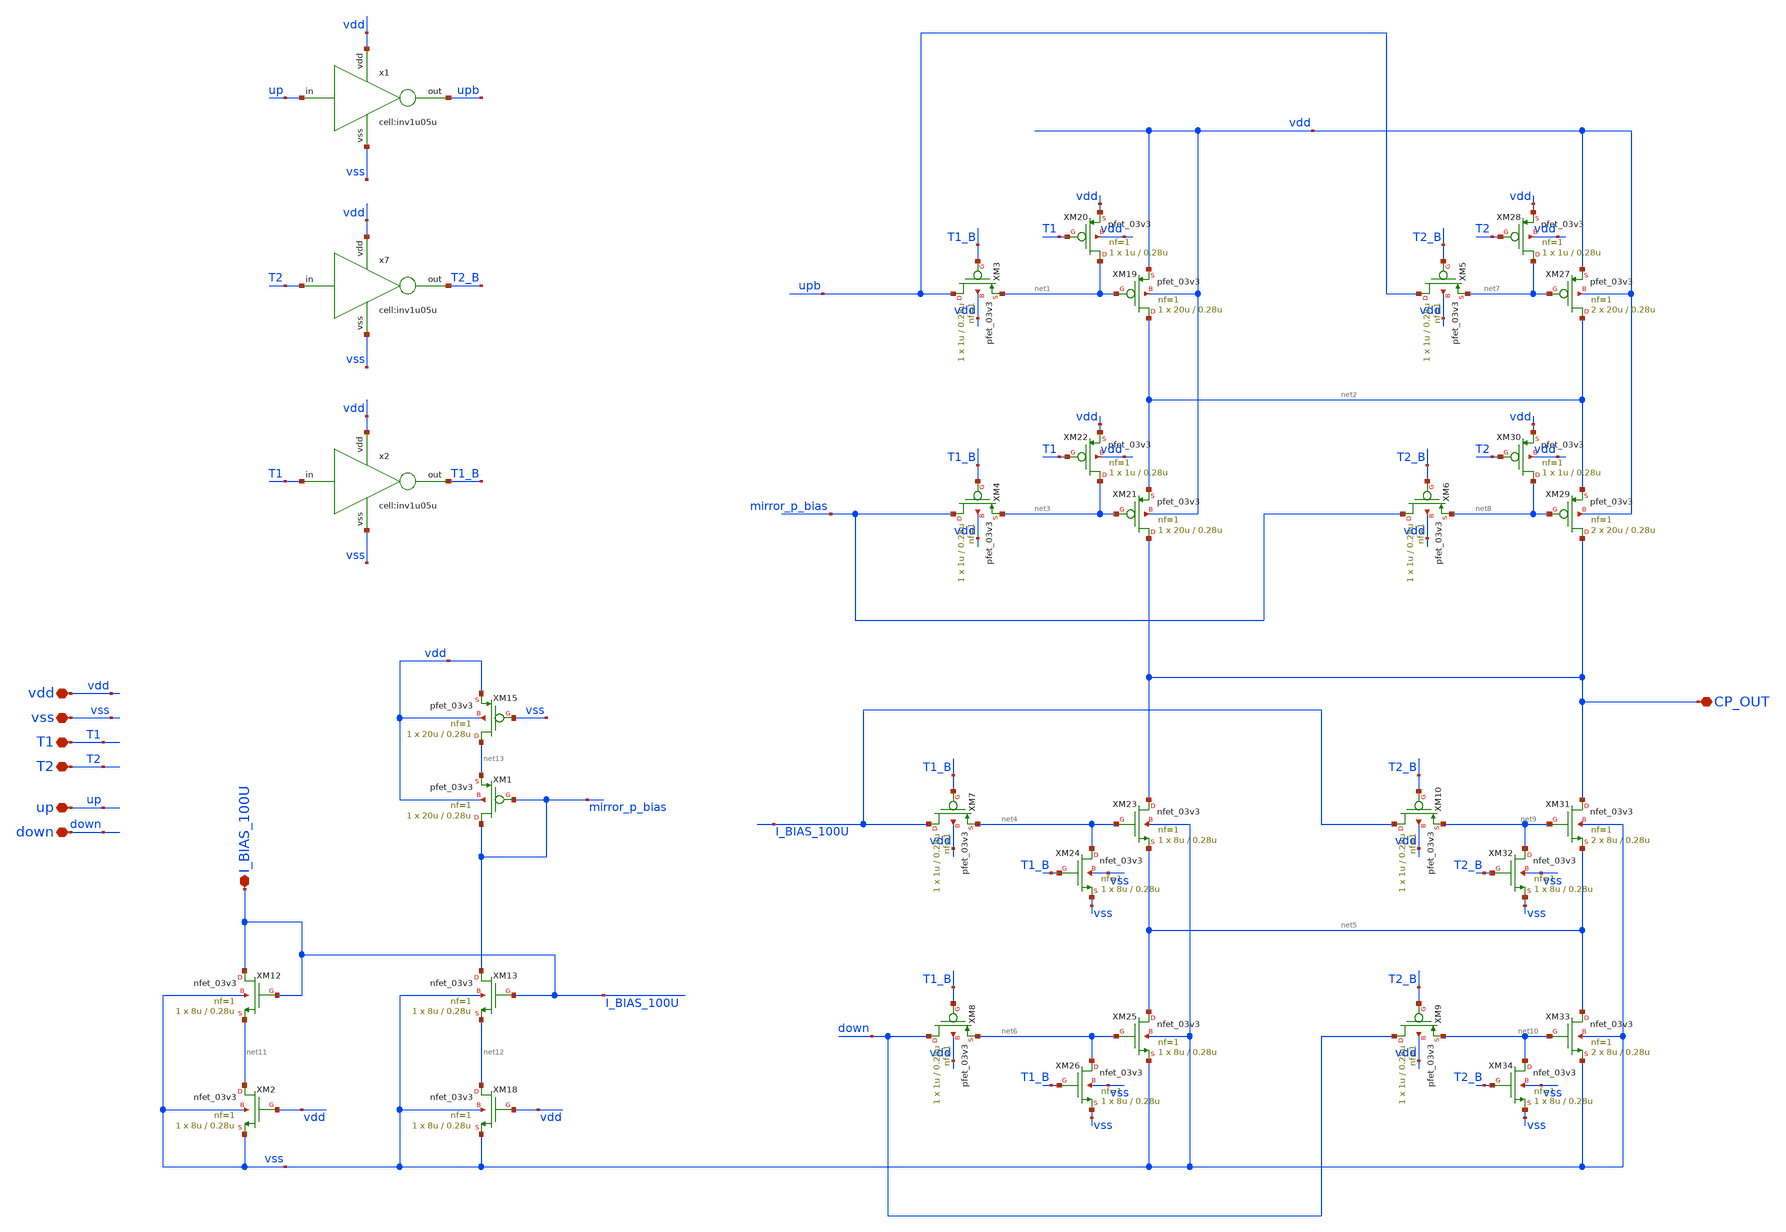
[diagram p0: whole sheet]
** sch_path: designs/libs/xp_core_analog/PGM_CP/PGM_CP.sch
**.subckt PGM_CP CP_OUT vdd vss T1 T2 I_BIAS_100U up down
*.iopin CP_OUT
*.iopin vdd
*.iopin vss
*.iopin T1
*.iopin T2
*.iopin I_BIAS_100U
*.iopin up
*.iopin down
XM2 net11 vdd vss vss nfet_03v3 L=0.28u W=8u nf=1 ad='int((nf+1)/2) * W/nf * 0.18u' as='int((nf+2)/2) * W/nf * 0.18u'
+ pd='2*int((nf+1)/2) * (W/nf + 0.18u)' ps='2*int((nf+2)/2) * (W/nf + 0.18u)' nrd='0.18u / W' nrs='0.18u / W'
+ sa=0 sb=0 sd=0 m=1
XM18 net12 vdd vss vss nfet_03v3 L=0.28u W=8u nf=1 ad='int((nf+1)/2) * W/nf * 0.18u' as='int((nf+2)/2) * W/nf * 0.18u'
+ pd='2*int((nf+1)/2) * (W/nf + 0.18u)' ps='2*int((nf+2)/2) * (W/nf + 0.18u)' nrd='0.18u / W' nrs='0.18u / W'
+ sa=0 sb=0 sd=0 m=1
XM19 net2 net1 vdd vdd pfet_03v3 L=0.28u W=20u nf=1 ad='int((nf+1)/2) * W/nf * 0.18u' as='int((nf+2)/2) * W/nf * 0.18u'
+ pd='2*int((nf+1)/2) * (W/nf + 0.18u)' ps='2*int((nf+2)/2) * (W/nf + 0.18u)' nrd='0.18u / W' nrs='0.18u / W'
+ sa=0 sb=0 sd=0 m=1
XM20 net1 T1 vdd vdd pfet_03v3 L=0.28u W=1u nf=1 ad='int((nf+1)/2) * W/nf * 0.18u' as='int((nf+2)/2) * W/nf * 0.18u'
+ pd='2*int((nf+1)/2) * (W/nf + 0.18u)' ps='2*int((nf+2)/2) * (W/nf + 0.18u)' nrd='0.18u / W' nrs='0.18u / W'
+ sa=0 sb=0 sd=0 m=1
XM21 CP_OUT net3 net2 vdd pfet_03v3 L=0.28u W=20u nf=1 ad='int((nf+1)/2) * W/nf * 0.18u' as='int((nf+2)/2) * W/nf * 0.18u'
+ pd='2*int((nf+1)/2) * (W/nf + 0.18u)' ps='2*int((nf+2)/2) * (W/nf + 0.18u)' nrd='0.18u / W' nrs='0.18u / W'
+ sa=0 sb=0 sd=0 m=1
XM22 net3 T1 vdd vdd pfet_03v3 L=0.28u W=1u nf=1 ad='int((nf+1)/2) * W/nf * 0.18u' as='int((nf+2)/2) * W/nf * 0.18u'
+ pd='2*int((nf+1)/2) * (W/nf + 0.18u)' ps='2*int((nf+2)/2) * (W/nf + 0.18u)' nrd='0.18u / W' nrs='0.18u / W'
+ sa=0 sb=0 sd=0 m=1
XM23 CP_OUT net4 net5 vss nfet_03v3 L=0.28u W=8u nf=1 ad='int((nf+1)/2) * W/nf * 0.18u' as='int((nf+2)/2) * W/nf * 0.18u'
+ pd='2*int((nf+1)/2) * (W/nf + 0.18u)' ps='2*int((nf+2)/2) * (W/nf + 0.18u)' nrd='0.18u / W' nrs='0.18u / W'
+ sa=0 sb=0 sd=0 m=1
XM24 net4 T1_B vss vss nfet_03v3 L=0.28u W=8u nf=1 ad='int((nf+1)/2) * W/nf * 0.18u' as='int((nf+2)/2) * W/nf * 0.18u'
+ pd='2*int((nf+1)/2) * (W/nf + 0.18u)' ps='2*int((nf+2)/2) * (W/nf + 0.18u)' nrd='0.18u / W' nrs='0.18u / W'
+ sa=0 sb=0 sd=0 m=1
XM25 net5 net6 vss vss nfet_03v3 L=0.28u W=8u nf=1 ad='int((nf+1)/2) * W/nf * 0.18u' as='int((nf+2)/2) * W/nf * 0.18u'
+ pd='2*int((nf+1)/2) * (W/nf + 0.18u)' ps='2*int((nf+2)/2) * (W/nf + 0.18u)' nrd='0.18u / W' nrs='0.18u / W'
+ sa=0 sb=0 sd=0 m=1
XM26 net6 T1_B vss vss nfet_03v3 L=0.28u W=8u nf=1 ad='int((nf+1)/2) * W/nf * 0.18u' as='int((nf+2)/2) * W/nf * 0.18u'
+ pd='2*int((nf+1)/2) * (W/nf + 0.18u)' ps='2*int((nf+2)/2) * (W/nf + 0.18u)' nrd='0.18u / W' nrs='0.18u / W'
+ sa=0 sb=0 sd=0 m=1
XM27 net2 net7 vdd vdd pfet_03v3 L=0.28u W=20u nf=1 ad='int((nf+1)/2) * W/nf * 0.18u' as='int((nf+2)/2) * W/nf * 0.18u'
+ pd='2*int((nf+1)/2) * (W/nf + 0.18u)' ps='2*int((nf+2)/2) * (W/nf + 0.18u)' nrd='0.18u / W' nrs='0.18u / W'
+ sa=0 sb=0 sd=0 m=2
XM28 net7 T2 vdd vdd pfet_03v3 L=0.28u W=1u nf=1 ad='int((nf+1)/2) * W/nf * 0.18u' as='int((nf+2)/2) * W/nf * 0.18u'
+ pd='2*int((nf+1)/2) * (W/nf + 0.18u)' ps='2*int((nf+2)/2) * (W/nf + 0.18u)' nrd='0.18u / W' nrs='0.18u / W'
+ sa=0 sb=0 sd=0 m=1
XM29 CP_OUT net8 net2 vdd pfet_03v3 L=0.28u W=20u nf=1 ad='int((nf+1)/2) * W/nf * 0.18u' as='int((nf+2)/2) * W/nf * 0.18u'
+ pd='2*int((nf+1)/2) * (W/nf + 0.18u)' ps='2*int((nf+2)/2) * (W/nf + 0.18u)' nrd='0.18u / W' nrs='0.18u / W'
+ sa=0 sb=0 sd=0 m=2
XM30 net8 T2 vdd vdd pfet_03v3 L=0.28u W=1u nf=1 ad='int((nf+1)/2) * W/nf * 0.18u' as='int((nf+2)/2) * W/nf * 0.18u'
+ pd='2*int((nf+1)/2) * (W/nf + 0.18u)' ps='2*int((nf+2)/2) * (W/nf + 0.18u)' nrd='0.18u / W' nrs='0.18u / W'
+ sa=0 sb=0 sd=0 m=1
XM31 CP_OUT net9 net5 vss nfet_03v3 L=0.28u W=8u nf=1 ad='int((nf+1)/2) * W/nf * 0.18u' as='int((nf+2)/2) * W/nf * 0.18u'
+ pd='2*int((nf+1)/2) * (W/nf + 0.18u)' ps='2*int((nf+2)/2) * (W/nf + 0.18u)' nrd='0.18u / W' nrs='0.18u / W'
+ sa=0 sb=0 sd=0 m=2
XM32 net9 T2_B vss vss nfet_03v3 L=0.28u W=8u nf=1 ad='int((nf+1)/2) * W/nf * 0.18u' as='int((nf+2)/2) * W/nf * 0.18u'
+ pd='2*int((nf+1)/2) * (W/nf + 0.18u)' ps='2*int((nf+2)/2) * (W/nf + 0.18u)' nrd='0.18u / W' nrs='0.18u / W'
+ sa=0 sb=0 sd=0 m=1
XM33 net5 net10 vss vss nfet_03v3 L=0.28u W=8u nf=1 ad='int((nf+1)/2) * W/nf * 0.18u' as='int((nf+2)/2) * W/nf * 0.18u'
+ pd='2*int((nf+1)/2) * (W/nf + 0.18u)' ps='2*int((nf+2)/2) * (W/nf + 0.18u)' nrd='0.18u / W' nrs='0.18u / W'
+ sa=0 sb=0 sd=0 m=2
XM34 net10 T2_B vss vss nfet_03v3 L=0.28u W=8u nf=1 ad='int((nf+1)/2) * W/nf * 0.18u' as='int((nf+2)/2) * W/nf * 0.18u'
+ pd='2*int((nf+1)/2) * (W/nf + 0.18u)' ps='2*int((nf+2)/2) * (W/nf + 0.18u)' nrd='0.18u / W' nrs='0.18u / W'
+ sa=0 sb=0 sd=0 m=1
XM12 I_BIAS_100U I_BIAS_100U net11 vss nfet_03v3 L=0.28u W=8u nf=1 ad='int((nf+1)/2) * W/nf * 0.18u'
+ as='int((nf+2)/2) * W/nf * 0.18u' pd='2*int((nf+1)/2) * (W/nf + 0.18u)' ps='2*int((nf+2)/2) * (W/nf + 0.18u)'
+ nrd='0.18u / W' nrs='0.18u / W' sa=0 sb=0 sd=0 m=1
XM13 mirror_p_bias I_BIAS_100U net12 vss nfet_03v3 L=0.28u W=8u nf=1 ad='int((nf+1)/2) * W/nf * 0.18u'
+ as='int((nf+2)/2) * W/nf * 0.18u' pd='2*int((nf+1)/2) * (W/nf + 0.18u)' ps='2*int((nf+2)/2) * (W/nf + 0.18u)'
+ nrd='0.18u / W' nrs='0.18u / W' sa=0 sb=0 sd=0 m=1
XM15 net13 vss vdd vdd pfet_03v3 L=0.28u W=20u nf=1 ad='int((nf+1)/2) * W/nf * 0.18u' as='int((nf+2)/2) * W/nf * 0.18u'
+ pd='2*int((nf+1)/2) * (W/nf + 0.18u)' ps='2*int((nf+2)/2) * (W/nf + 0.18u)' nrd='0.18u / W' nrs='0.18u / W'
+ sa=0 sb=0 sd=0 m=1
x1 up vdd upb vss inv1u05u
x7 T2 vdd T2_B vss inv1u05u
x2 T1 vdd T1_B vss inv1u05u
XM1 mirror_p_bias mirror_p_bias net13 vdd pfet_03v3 L=0.28u W=20u nf=1 ad='int((nf+1)/2) * W/nf * 0.18u'
+ as='int((nf+2)/2) * W/nf * 0.18u' pd='2*int((nf+1)/2) * (W/nf + 0.18u)' ps='2*int((nf+2)/2) * (W/nf + 0.18u)'
+ nrd='0.18u / W' nrs='0.18u / W' sa=0 sb=0 sd=0 m=1
XM3 upb T1_B net1 vdd pfet_03v3 L=0.28u W=1u nf=1 ad='int((nf+1)/2) * W/nf * 0.18u' as='int((nf+2)/2) * W/nf * 0.18u'
+ pd='2*int((nf+1)/2) * (W/nf + 0.18u)' ps='2*int((nf+2)/2) * (W/nf + 0.18u)' nrd='0.18u / W' nrs='0.18u / W'
+ sa=0 sb=0 sd=0 m=1
XM4 mirror_p_bias T1_B net3 vdd pfet_03v3 L=0.28u W=1u nf=1 ad='int((nf+1)/2) * W/nf * 0.18u' as='int((nf+2)/2) * W/nf * 0.18u'
+ pd='2*int((nf+1)/2) * (W/nf + 0.18u)' ps='2*int((nf+2)/2) * (W/nf + 0.18u)' nrd='0.18u / W' nrs='0.18u / W'
+ sa=0 sb=0 sd=0 m=1
XM5 upb T2_B net7 vdd pfet_03v3 L=0.28u W=1u nf=1 ad='int((nf+1)/2) * W/nf * 0.18u' as='int((nf+2)/2) * W/nf * 0.18u'
+ pd='2*int((nf+1)/2) * (W/nf + 0.18u)' ps='2*int((nf+2)/2) * (W/nf + 0.18u)' nrd='0.18u / W' nrs='0.18u / W'
+ sa=0 sb=0 sd=0 m=1
XM6 mirror_p_bias T2_B net8 vdd pfet_03v3 L=0.28u W=1u nf=1 ad='int((nf+1)/2) * W/nf * 0.18u' as='int((nf+2)/2) * W/nf * 0.18u'
+ pd='2*int((nf+1)/2) * (W/nf + 0.18u)' ps='2*int((nf+2)/2) * (W/nf + 0.18u)' nrd='0.18u / W' nrs='0.18u / W'
+ sa=0 sb=0 sd=0 m=1
XM7 I_BIAS_100U T1_B net4 vdd pfet_03v3 L=0.28u W=1u nf=1 ad='int((nf+1)/2) * W/nf * 0.18u' as='int((nf+2)/2) * W/nf * 0.18u'
+ pd='2*int((nf+1)/2) * (W/nf + 0.18u)' ps='2*int((nf+2)/2) * (W/nf + 0.18u)' nrd='0.18u / W' nrs='0.18u / W'
+ sa=0 sb=0 sd=0 m=1
XM8 down T1_B net6 vdd pfet_03v3 L=0.28u W=1u nf=1 ad='int((nf+1)/2) * W/nf * 0.18u' as='int((nf+2)/2) * W/nf * 0.18u'
+ pd='2*int((nf+1)/2) * (W/nf + 0.18u)' ps='2*int((nf+2)/2) * (W/nf + 0.18u)' nrd='0.18u / W' nrs='0.18u / W'
+ sa=0 sb=0 sd=0 m=1
XM9 down T2_B net10 vdd pfet_03v3 L=0.28u W=1u nf=1 ad='int((nf+1)/2) * W/nf * 0.18u' as='int((nf+2)/2) * W/nf * 0.18u'
+ pd='2*int((nf+1)/2) * (W/nf + 0.18u)' ps='2*int((nf+2)/2) * (W/nf + 0.18u)' nrd='0.18u / W' nrs='0.18u / W'
+ sa=0 sb=0 sd=0 m=1
XM10 I_BIAS_100U T2_B net9 vdd pfet_03v3 L=0.28u W=1u nf=1 ad='int((nf+1)/2) * W/nf * 0.18u' as='int((nf+2)/2) * W/nf * 0.18u'
+ pd='2*int((nf+1)/2) * (W/nf + 0.18u)' ps='2*int((nf+2)/2) * (W/nf + 0.18u)' nrd='0.18u / W' nrs='0.18u / W'
+ sa=0 sb=0 sd=0 m=1
**.ends
.end
